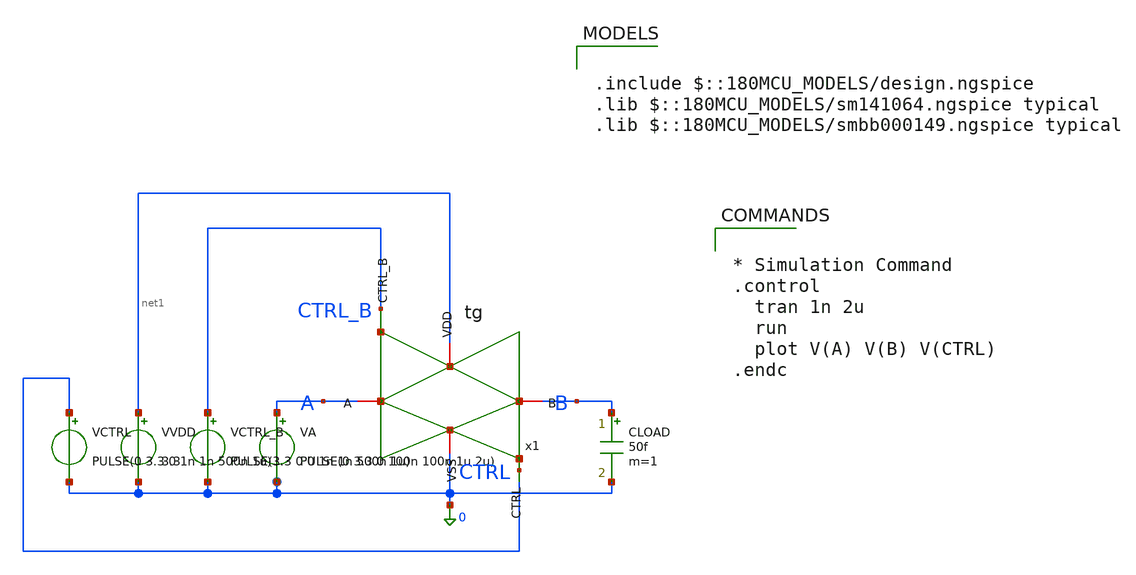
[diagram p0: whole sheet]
** sch_path: sar_logic/sar_designs/tb_tg.sch
**.subckt tb_tg
x1 CTRL 0 A B net1 CTRL_B tg
VCTRL CTRL 0 PULSE(0 3.3 0 1n 1n 500n 1u)
VA A 0 PULSE(0 3.3 0 100n 100n 1u 2u)
VCTRL_B CTRL_B 0 PULSE(3.3 0 0 1n 1n 500n 1u)
VVDD net1 0 3.3
CLOAD B 0 50f m=1
**** begin user architecture code

.include $::180MCU_MODELS/design.ngspice
.lib $::180MCU_MODELS/sm141064.ngspice typical
.lib $::180MCU_MODELS/smbb000149.ngspice typical



* Simulation Command
.control
  tran 1n 2u
  run
  plot V(A) V(B) V(CTRL)
.endc

**** end user architecture code
**.ends

* expanding   symbol:  tg.sym # of pins=6
** sym_path: sar_logic/sar_designs/tg.sym
** sch_path: sar_logic/sar_designs/tg.sch
.subckt tg CTRL VSS A B VDD CTRL_B
*.iopin VDD
*.iopin VSS
*.iopin A
*.iopin B
*.ipin CTRL_B
*.ipin CTRL
XM1 A CTRL_B B VDD pfet_03v3 L=1u W=0.28u nf=1 ad='int((nf+1)/2) * W/nf * 0.18u' as='int((nf+2)/2) * W/nf * 0.18u'
+ pd='2*int((nf+1)/2) * (W/nf + 0.18u)' ps='2*int((nf+2)/2) * (W/nf + 0.18u)' nrd='0.18u / W' nrs='0.18u / W'
+ sa=0 sb=0 sd=0 m=1
XM2 A CTRL B VSS nfet_03v3 L=0.28u W=0.5u nf=1 ad='int((nf+1)/2) * W/nf * 0.18u' as='int((nf+2)/2) * W/nf * 0.18u'
+ pd='2*int((nf+1)/2) * (W/nf + 0.18u)' ps='2*int((nf+2)/2) * (W/nf + 0.18u)' nrd='0.18u / W' nrs='0.18u / W'
+ sa=0 sb=0 sd=0 m=1
.ends

.end
